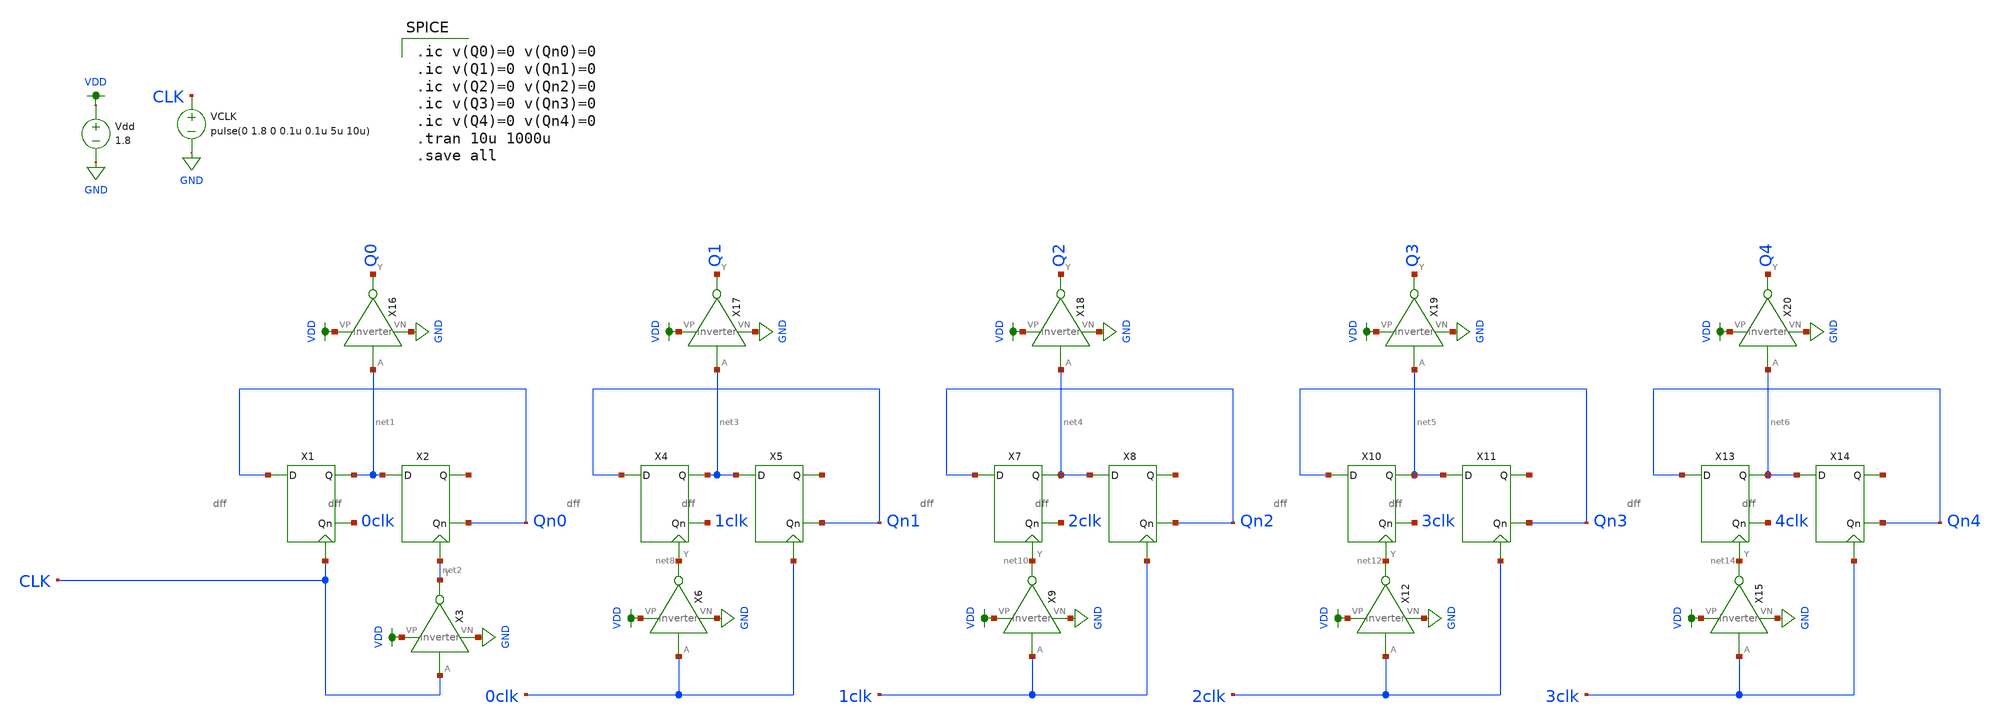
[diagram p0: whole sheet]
** sch_path: schematic/counter_new.sch
**.subckt counter_new
Vdd VDD GND 1.8
VCLK CLK GND pulse(0 1.8 0 0.1u 0.1u 5u 10u)
X1 Qn0 0clk net1 CLK dff
X2 net1 Qn0 net7 net2 dff
X3 CLK net2 VDD GND inverter
X4 Qn1 1clk net3 net8 dff
X5 net3 Qn1 net9 0clk dff
X6 0clk net8 VDD GND inverter
X7 Qn2 2clk net4 net10 dff
X8 net4 Qn2 net11 1clk dff
X10 Qn3 3clk net5 net12 dff
X11 net5 Qn3 net13 2clk dff
X13 Qn4 4clk net6 net14 dff
X14 net6 Qn4 net15 3clk dff
X9 1clk net10 VDD GND inverter
X12 2clk net12 VDD GND inverter
X15 3clk net14 VDD GND inverter
X16 net1 Q0 VDD GND inverter
X17 net3 Q1 VDD GND inverter
X18 net4 Q2 VDD GND inverter
X19 net5 Q3 VDD GND inverter
X20 net6 Q4 VDD GND inverter
**** begin user architecture code

.ic v(Q0)=0 v(Qn0)=0
.ic v(Q1)=0 v(Qn1)=0
.ic v(Q2)=0 v(Qn2)=0
.ic v(Q3)=0 v(Qn3)=0
.ic v(Q4)=0 v(Qn4)=0
.tran 10u 1000u
.save all


.option wnflag=1
.param MC_SWITCH=0.0
.lib ~/skywater/skywater-pdk/libraries/sky130_fd_pr_ngspice/latest/models/sky130.lib.spice tt

**** end user architecture code
**.ends

* expanding   symbol:  /home/madvlsi/Documents/MADVLSI-Final_Project/schematic/dff.sym # of pins=4
** sym_path: schematic/dff.sym
** sch_path: schematic/dff.sch
.subckt dff D Qn Q CLK
*.ipin D
*.iopin CLK
*.opin Qn
*.opin Q
X2 D CLK net1 VDD GND nand2
X3 net3 CLK net2 VDD GND nand2
X4 Q net2 Qn VDD GND nand2
X5 net1 Qn Q VDD GND nand2
X1 D net3 VDD GND inverter
.ends


* expanding   symbol:  /home/madvlsi/Documents/MADVLSI-Final_Project/schematic/inverter.sym # of
*+ pins=4
** sym_path: schematic/inverter.sym
** sch_path: schematic/inverter.sch
.subckt inverter A Y VP VN
*.opin Y
*.ipin A
*.iopin VP
*.iopin VN
XM3 Y A VP VDD sky130_fd_pr__pfet_01v8 L={Lp} W={Wp} nf=1 ad='int((nf+1)/2) * W/nf * 0.29' as='int((nf+2)/2) * W/nf * 0.29'
+ pd='2*int((nf+1)/2) * (W/nf + 0.29)' ps='2*int((nf+2)/2) * (W/nf + 0.29)' nrd='0.29 / W' nrs='0.29 / W'
+ sa=0 sb=0 sd=0 mult=1 m=1
XM4 Y A VP VDD sky130_fd_pr__pfet_01v8 L={Lp} W={Wp} nf=1 ad='int((nf+1)/2) * W/nf * 0.29' as='int((nf+2)/2) * W/nf * 0.29'
+ pd='2*int((nf+1)/2) * (W/nf + 0.29)' ps='2*int((nf+2)/2) * (W/nf + 0.29)' nrd='0.29 / W' nrs='0.29 / W'
+ sa=0 sb=0 sd=0 mult=1 m=1
XM5 Y A VN GND sky130_fd_pr__nfet_01v8 L={Lp} W={Wp} nf=1 ad='int((nf+1)/2) * W/nf * 0.29' as='int((nf+2)/2) * W/nf * 0.29'
+ pd='2*int((nf+1)/2) * (W/nf + 0.29)' ps='2*int((nf+2)/2) * (W/nf + 0.29)' nrd='0.29 / W' nrs='0.29 / W'
+ sa=0 sb=0 sd=0 mult=1 m=1
.ends


* expanding   symbol:  /home/madvlsi/Documents/MADVLSI-Final_Project/schematic/nand2.sym # of pins=5
** sym_path: schematic/nand2.sym
** sch_path: schematic/nand2.sch
.subckt nand2 A B Y VP VN
*.ipin A
*.opin Y
*.ipin B
*.iopin VP
*.iopin VP
*.iopin VN
*.iopin VN
XM1 Y A VP VP sky130_fd_pr__pfet_01v8 L=0.15 W=2 nf=1 ad='int((nf+1)/2) * W/nf * 0.29' as='int((nf+2)/2) * W/nf * 0.29'
+ pd='2*int((nf+1)/2) * (W/nf + 0.29)' ps='2*int((nf+2)/2) * (W/nf + 0.29)' nrd='0.29 / W' nrs='0.29 / W'
+ sa=0 sb=0 sd=0 mult=1 m=1
XM2 VP B Y VP sky130_fd_pr__pfet_01v8 L=0.15 W=2 nf=1 ad='int((nf+1)/2) * W/nf * 0.29' as='int((nf+2)/2) * W/nf * 0.29'
+ pd='2*int((nf+1)/2) * (W/nf + 0.29)' ps='2*int((nf+2)/2) * (W/nf + 0.29)' nrd='0.29 / W' nrs='0.29 / W'
+ sa=0 sb=0 sd=0 mult=1 m=1
XM3 net1 B Y VN sky130_fd_pr__nfet_01v8 L=0.15 W=2 nf=1 ad='int((nf+1)/2) * W/nf * 0.29' as='int((nf+2)/2) * W/nf * 0.29'
+ pd='2*int((nf+1)/2) * (W/nf + 0.29)' ps='2*int((nf+2)/2) * (W/nf + 0.29)' nrd='0.29 / W' nrs='0.29 / W'
+ sa=0 sb=0 sd=0 mult=1 m=1
XM4 net1 A VN VN sky130_fd_pr__nfet_01v8 L=0.15 W=2 nf=1 ad='int((nf+1)/2) * W/nf * 0.29' as='int((nf+2)/2) * W/nf * 0.29'
+ pd='2*int((nf+1)/2) * (W/nf + 0.29)' ps='2*int((nf+2)/2) * (W/nf + 0.29)' nrd='0.29 / W' nrs='0.29 / W'
+ sa=0 sb=0 sd=0 mult=1 m=1
.ends

.GLOBAL GND
.GLOBAL VDD
.end
